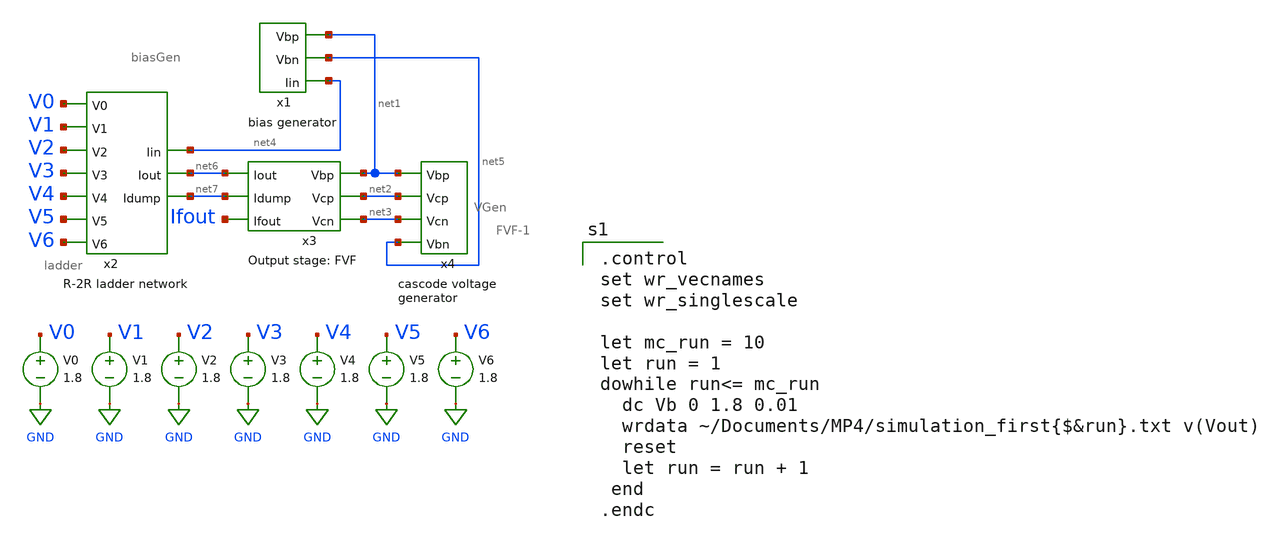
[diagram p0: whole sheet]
** sch_path: MP4-simulation-1.sch
**.subckt MP4-simulation-1
x1 net1 net4 net5 biasGen
V1 V1 GND 1.8
V2 V2 GND 1.8
V3 V3 GND 1.8
V4 V4 GND 1.8
V5 V5 GND 1.8
V6 V6 GND 1.8
V0 V0 GND 1.8
x2 net4 net7 net6 V0 V1 V2 V3 V4 V5 V6 ladder
x3 net1 net2 net6 net3 Ifout net7 FVF-1
x4 net1 net3 net2 net5 VGen
**** begin user architecture code

.option wnflag=1
.param MC_SWITCH=0.0
.lib ~/skywater/skywater-pdk/libraries/sky130_fd_pr_ngspice/latest/models/sky130.lib.spice tt


.control
set wr_vecnames
set wr_singlescale

let mc_run = 10
let run = 1
dowhile run<= mc_run
  dc Vb 0 1.8 0.01
  wrdata ~/Documents/MP4/simulation_first{$&run}.txt v(Vout)
  reset
  let run = run + 1
 end
.endc

**** end user architecture code
**.ends
.GLOBAL GND
.end
